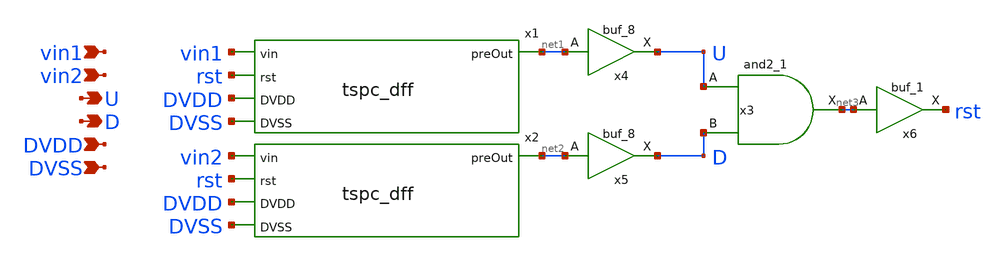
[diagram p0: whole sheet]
** sch_path: xschem/pfd.sch
**.subckt pfd vin1 vin2 U D DVDD DVSS
*.ipin vin1
*.ipin vin2
*.opin U
*.opin D
*.ipin DVDD
*.ipin DVSS
x3 U D DVSS DVSS DVDD DVDD net3 sky130_fd_sc_hd__and2_1
x4 net1 DVSS DVSS DVDD DVDD U sky130_fd_sc_hd__buf_8
x5 net2 DVSS DVSS DVDD DVDD D sky130_fd_sc_hd__buf_8
x6 net3 DVSS DVSS DVDD DVDD rst sky130_fd_sc_hd__buf_1
x1 vin1 rst net1 DVDD DVSS tspc_dff
x2 vin2 rst net2 DVDD DVSS tspc_dff
**.ends

* expanding   symbol:  /home/gils/aic/sky130_its_biomedical_chip_research_2024/xschem/tspc_dff.sym #
*+ of pins=5
** sym_path: xschem/tspc_dff.sym
** sch_path: xschem/tspc_dff.sch
.subckt tspc_dff vin rst preOut DVDD DVSS
*.ipin vin
*.ipin rst
*.opin preOut
*.ipin DVDD
*.ipin DVSS
x1 rst vin net1 net2 preOut DVDD pcell_pfd
x2 rst vin net1 net2 preOut DVSS ncell_pfd
.ends


* expanding   symbol:  /home/gils/aic/sky130_its_biomedical_chip_research_2024/xschem/pcell_pfd.sym
*+ # of pins=6
** sym_path: xschem/pcell_pfd.sym
** sch_path: xschem/pcell_pfd.sch
.subckt pcell_pfd rst vin drain1 drain2 preOut DVDD
*.ipin rst
*.ipin vin
*.ipin drain1
*.ipin drain2
*.opin preOut
*.ipin DVDD
XM1 net1 vin DVDD DVDD sky130_fd_pr__pfet_01v8 L=0.15 W=1.26 nf=1 ad='int((nf+1)/2) * W/nf * 0.29' as='int((nf+2)/2) * W/nf * 0.29'
+ pd='2*int((nf+1)/2) * (W/nf + 0.29)' ps='2*int((nf+2)/2) * (W/nf + 0.29)' nrd='0.29 / W' nrs='0.29 / W'
+ sa=0 sb=0 sd=0 mult=1 m=1
XM2 drain1 rst net1 DVDD sky130_fd_pr__pfet_01v8 L=0.15 W=1.26 nf=1 ad='int((nf+1)/2) * W/nf * 0.29'
+ as='int((nf+2)/2) * W/nf * 0.29' pd='2*int((nf+1)/2) * (W/nf + 0.29)' ps='2*int((nf+2)/2) * (W/nf + 0.29)'
+ nrd='0.29 / W' nrs='0.29 / W' sa=0 sb=0 sd=0 mult=1 m=1
XM3 drain2 drain1 DVDD DVDD sky130_fd_pr__pfet_01v8 L=0.15 W=1.26 nf=1 ad='int((nf+1)/2) * W/nf * 0.29'
+ as='int((nf+2)/2) * W/nf * 0.29' pd='2*int((nf+1)/2) * (W/nf + 0.29)' ps='2*int((nf+2)/2) * (W/nf + 0.29)'
+ nrd='0.29 / W' nrs='0.29 / W' sa=0 sb=0 sd=0 mult=1 m=1
XM4 preOut drain2 DVDD DVDD sky130_fd_pr__pfet_01v8 L=0.15 W=1.26 nf=1 ad='int((nf+1)/2) * W/nf * 0.29'
+ as='int((nf+2)/2) * W/nf * 0.29' pd='2*int((nf+1)/2) * (W/nf + 0.29)' ps='2*int((nf+2)/2) * (W/nf + 0.29)'
+ nrd='0.29 / W' nrs='0.29 / W' sa=0 sb=0 sd=0 mult=1 m=1
.ends


* expanding   symbol:  /home/gils/aic/sky130_its_biomedical_chip_research_2024/xschem/ncell_pfd.sym
*+ # of pins=6
** sym_path: xschem/ncell_pfd.sym
** sch_path: xschem/ncell_pfd.sch
.subckt ncell_pfd rst vin drain1 drain2 preOut DVSS
*.ipin rst
*.ipin vin
*.ipin drain1
*.ipin drain2
*.opin preOut
*.ipin DVSS
XM1 drain1 rst DVSS DVSS sky130_fd_pr__nfet_01v8 L=0.15 W=0.42 nf=1 ad='int((nf+1)/2) * W/nf * 0.29'
+ as='int((nf+2)/2) * W/nf * 0.29' pd='2*int((nf+1)/2) * (W/nf + 0.29)' ps='2*int((nf+2)/2) * (W/nf + 0.29)'
+ nrd='0.29 / W' nrs='0.29 / W' sa=0 sb=0 sd=0 mult=1 m=1
XM2 net1 vin DVSS DVSS sky130_fd_pr__nfet_01v8 L=0.15 W=0.42 nf=1 ad='int((nf+1)/2) * W/nf * 0.29' as='int((nf+2)/2) * W/nf * 0.29'
+ pd='2*int((nf+1)/2) * (W/nf + 0.29)' ps='2*int((nf+2)/2) * (W/nf + 0.29)' nrd='0.29 / W' nrs='0.29 / W'
+ sa=0 sb=0 sd=0 mult=1 m=1
XM3 preOut drain2 DVSS DVSS sky130_fd_pr__nfet_01v8 L=0.15 W=0.42 nf=1 ad='int((nf+1)/2) * W/nf * 0.29'
+ as='int((nf+2)/2) * W/nf * 0.29' pd='2*int((nf+1)/2) * (W/nf + 0.29)' ps='2*int((nf+2)/2) * (W/nf + 0.29)'
+ nrd='0.29 / W' nrs='0.29 / W' sa=0 sb=0 sd=0 mult=1 m=1
XM4 drain2 drain1 net1 DVSS sky130_fd_pr__nfet_01v8 L=0.15 W=0.42 nf=1 ad='int((nf+1)/2) * W/nf * 0.29'
+ as='int((nf+2)/2) * W/nf * 0.29' pd='2*int((nf+1)/2) * (W/nf + 0.29)' ps='2*int((nf+2)/2) * (W/nf + 0.29)'
+ nrd='0.29 / W' nrs='0.29 / W' sa=0 sb=0 sd=0 mult=1 m=1
.ends

.end
